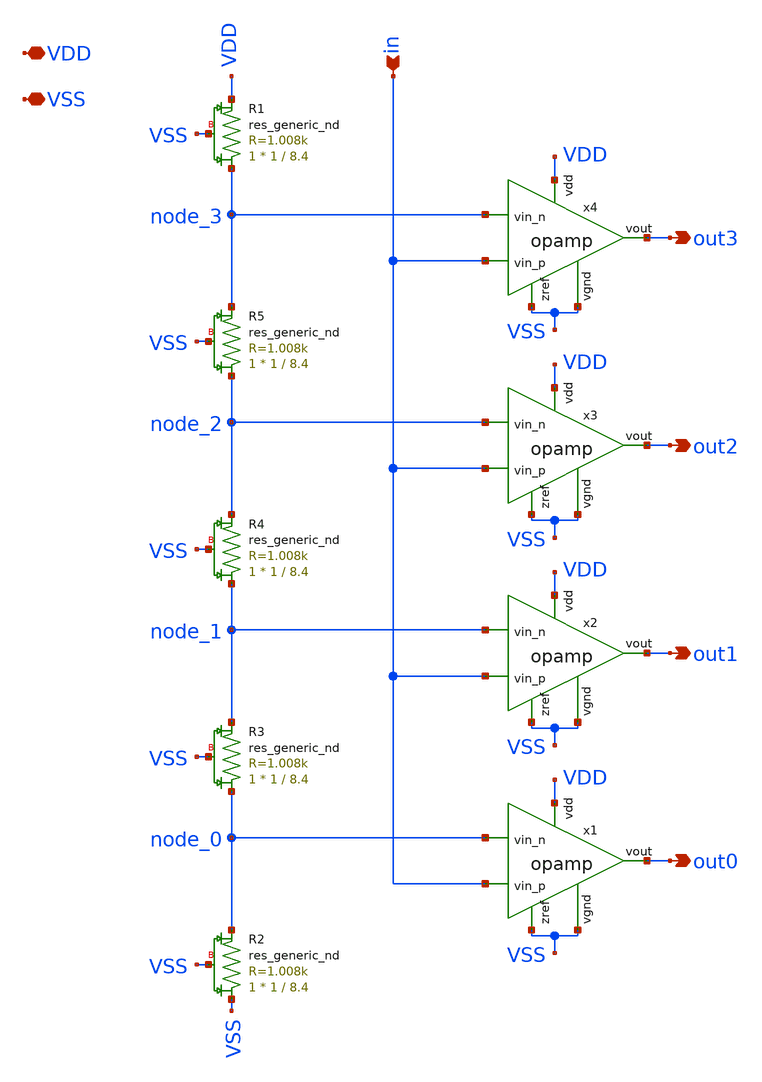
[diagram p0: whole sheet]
** sch_path: xschem/opamp_ladder.sch
**.subckt opamp_ladder out0 out2 out3 in VDD VSS out1
*.opin out0
*.opin out2
*.opin out3
*.ipin in
*.iopin VDD
*.iopin VSS
*.opin out1
x1 VDD VSS node_0 in out0 VSS opamp
XR2 VSS node_0 VSS sky130_fd_pr__res_generic_nd W=1 L=8.4 mult=1 m=1
XR3 node_0 node_1 VSS sky130_fd_pr__res_generic_nd W=1 L=8.4 mult=1 m=1
XR4 node_1 node_2 VSS sky130_fd_pr__res_generic_nd W=1 L=8.4 mult=1 m=1
XR5 node_2 node_3 VSS sky130_fd_pr__res_generic_nd W=1 L=8.4 mult=1 m=1
x2 VDD VSS node_1 in out1 VSS opamp
x3 VDD VSS node_2 in out2 VSS opamp
x4 VDD VSS node_3 in out3 VSS opamp
XR1 node_3 VDD VSS sky130_fd_pr__res_generic_nd W=1 L=8.4 mult=1 m=1
**.ends

* expanding   symbol:  opamp.sym # of pins=6
** sym_path: xschem/opamp.sym
** sch_path: xschem/opamp.sch
.subckt opamp VDD ZREF vin_n vin_p Vout VGND
*.ipin vin_n
*.ipin vin_p
*.opin Vout
*.iopin VDD
*.iopin ZREF
*.iopin VGND
XM1 net1 vin_n net3 net3 sky130_fd_pr__pfet_01v8 L=0.6 W=6 nf=1 ad='W * 0.29' as='W * 0.29' pd='2 * (W + 0.29)'
+ ps='2 * (W + 0.29)' nrd='0.29 / W' nrs='0.29 / W' sa=0 sb=0 sd=0 mult=1 m=1
XM2 net2 vin_p net3 net3 sky130_fd_pr__pfet_01v8 L=0.6 W=6 nf=1 ad='W * 0.29' as='W * 0.29' pd='2 * (W + 0.29)'
+ ps='2 * (W + 0.29)' nrd='0.29 / W' nrs='0.29 / W' sa=0 sb=0 sd=0 mult=1 m=1
XM3 net1 net1 VGND VGND sky130_fd_pr__nfet_01v8 L=0.6 W=6 nf=1 ad='W * 0.29' as='W * 0.29' pd='2 * (W + 0.29)'
+ ps='2 * (W + 0.29)' nrd='0.29 / W' nrs='0.29 / W' sa=0 sb=0 sd=0 mult=1 m=1
XM4 net2 net1 VGND VGND sky130_fd_pr__nfet_01v8 L=0.6 W=6 nf=1 ad='W * 0.29' as='W * 0.29' pd='2 * (W + 0.29)'
+ ps='2 * (W + 0.29)' nrd='0.29 / W' nrs='0.29 / W' sa=0 sb=0 sd=0 mult=1 m=1
XM5 net3 VGND VDD VDD sky130_fd_pr__pfet_01v8 L=0.6 W=6 nf=1 ad='W * 0.29' as='W * 0.29' pd='2 * (W + 0.29)'
+ ps='2 * (W + 0.29)' nrd='0.29 / W' nrs='0.29 / W' sa=0 sb=0 sd=0 mult=1 m=1
XM7 Vout VGND VDD VDD sky130_fd_pr__pfet_01v8 L=0.6 W=6 nf=1 ad='W * 0.29' as='W * 0.29' pd='2 * (W + 0.29)'
+ ps='2 * (W + 0.29)' nrd='0.29 / W' nrs='0.29 / W' sa=0 sb=0 sd=0 mult=1 m=1
XM8 ZREF VGND VDD VDD sky130_fd_pr__pfet_01v8 L=0.6 W=6 nf=1 ad='W * 0.29' as='W * 0.29' pd='2 * (W + 0.29)'
+ ps='2 * (W + 0.29)' nrd='0.29 / W' nrs='0.29 / W' sa=0 sb=0 sd=0 mult=1 m=1
XM9 net4 VDD net2 VGND sky130_fd_pr__nfet_01v8 L=0.6 W=1 nf=1 ad='W * 0.29' as='W * 0.29' pd='2 * (W + 0.29)'
+ ps='2 * (W + 0.29)' nrd='0.29 / W' nrs='0.29 / W' sa=0 sb=0 sd=0 mult=1 m=1
XC1 net4 Vout sky130_fd_pr__cap_mim_m3_1 W=17.55 L=15 MF=1 m=1
XM6 Vout net2 VGND VGND sky130_fd_pr__nfet_01v8 L=0.6 W=6 nf=1 ad='W * 0.29' as='W * 0.29' pd='2 * (W + 0.29)'
+ ps='2 * (W + 0.29)' nrd='0.29 / W' nrs='0.29 / W' sa=0 sb=0 sd=0 mult=1 m=1
XR1 ZREF VDD VGND sky130_fd_pr__res_generic_nd W=1 L=5 mult=1 m=1
XR2 VGND ZREF VGND sky130_fd_pr__res_generic_nd W=1 L=5 mult=1 m=1
.ends

.end
